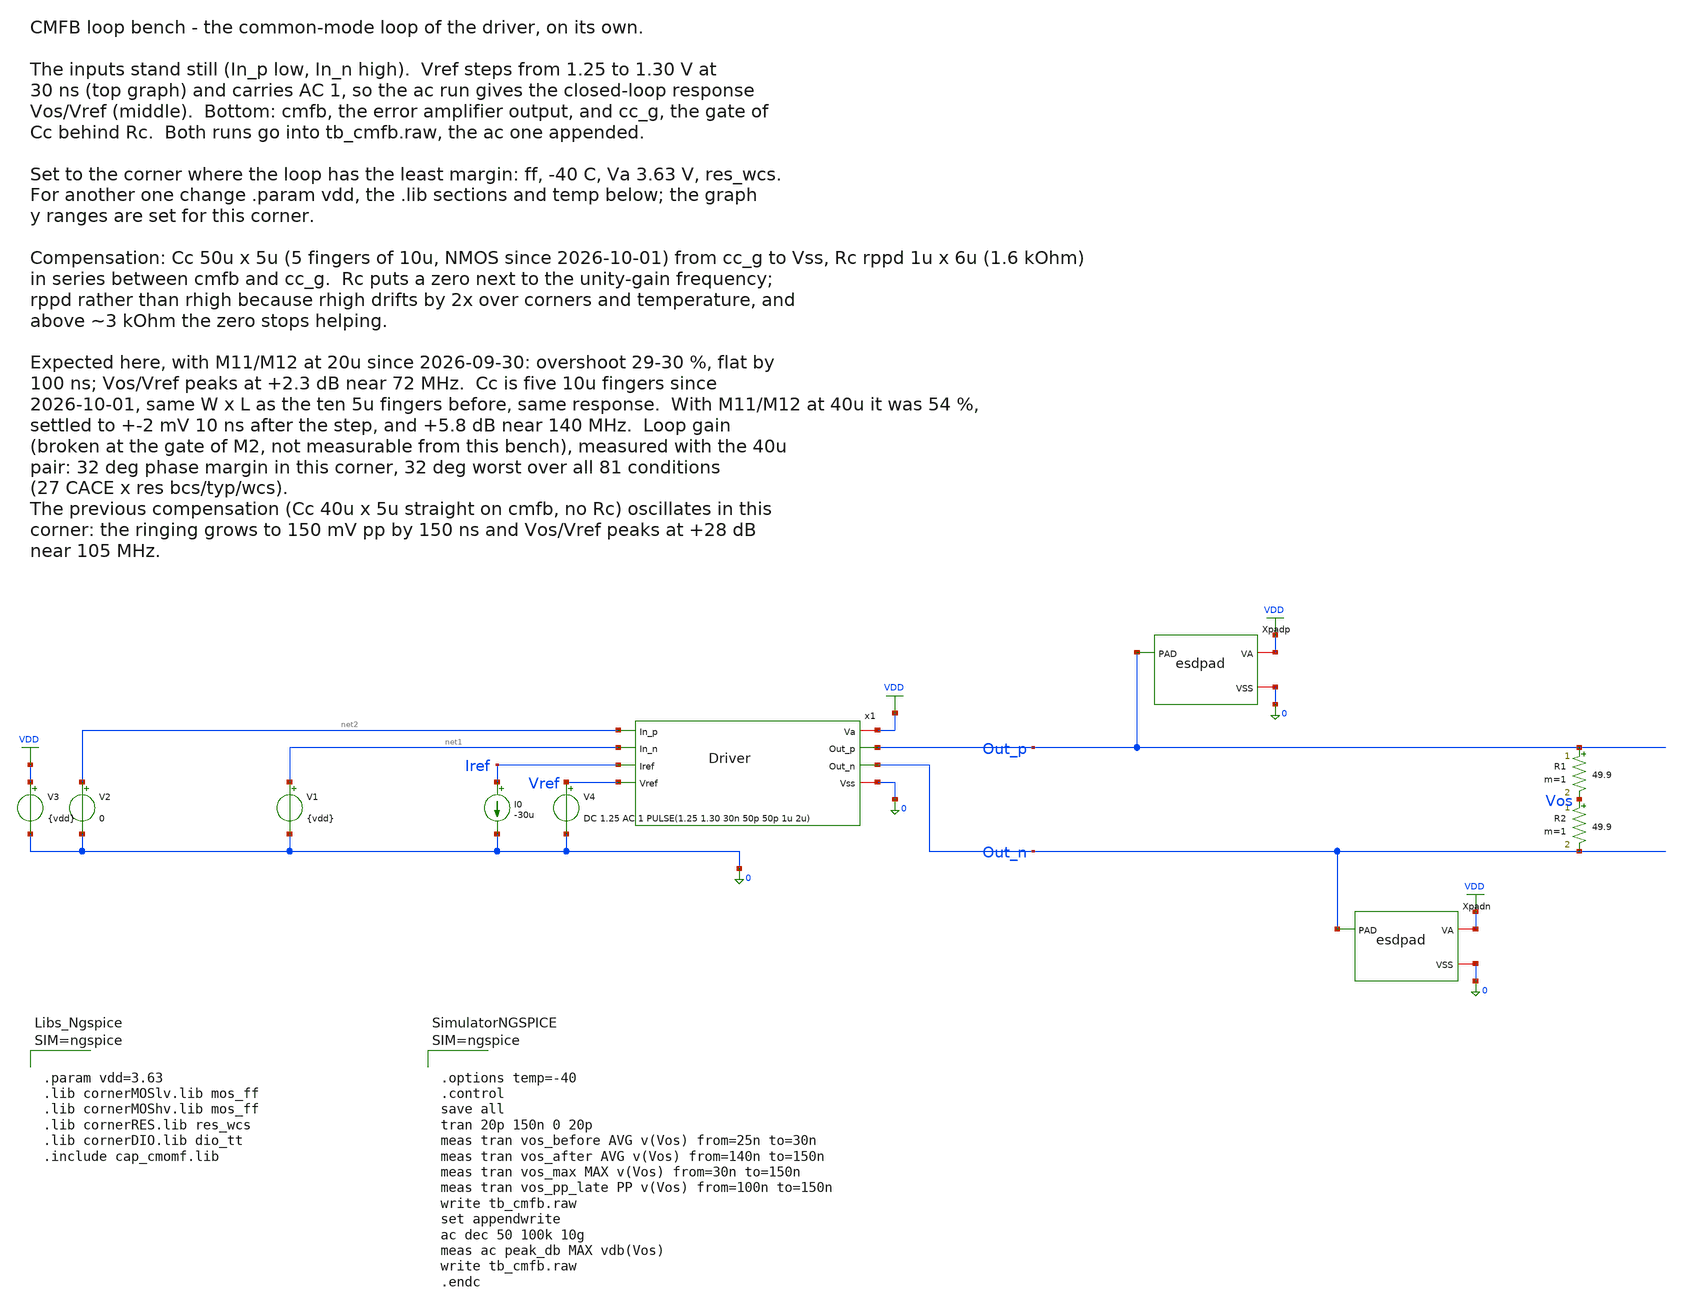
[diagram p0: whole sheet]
** sch_path: macros/lvds_tx/testbenches/xschem/tb_cmfb.sch
**.subckt tb_cmfb
x1 VDD Out_p net2 net1 Iref Vref Out_n 0 Driver
Xpadp Out_p VDD 0 esdpad
Xpadn Out_n VDD 0 esdpad
R1 Out_p Vos 49.9 m=1
R2 Vos Out_n 49.9 m=1
I0 Iref 0 -30u
V1 net1 0 {vdd}
V2 net2 0 0
V3 VDD 0 {vdd}
V4 Vref 0 DC 1.25 AC 1 PULSE(1.25 1.30 30n 50p 50p 1u 2u)
**** begin user architecture code



.param vdd=3.63
.lib cornerMOSlv.lib mos_ff
.lib cornerMOShv.lib mos_ff
.lib cornerRES.lib res_wcs
.lib cornerDIO.lib dio_tt
.include cap_cmomf.lib






.options temp=-40
.control
save all
tran 20p 150n 0 20p
meas tran vos_before AVG v(Vos) from=25n to=30n
meas tran vos_after AVG v(Vos) from=140n to=150n
meas tran vos_max MAX v(Vos) from=30n to=150n
meas tran vos_pp_late PP v(Vos) from=100n to=150n
write tb_cmfb.raw
set appendwrite
ac dec 50 100k 10g
meas ac peak_db MAX vdb(Vos)
write tb_cmfb.raw
.endc



**** end user architecture code
**.ends

* expanding   symbol:  Driver.sym # of pins=8
** sym_path: macros/lvds_tx/schematic/xschem/Driver.sym
** sch_path: macros/lvds_tx/schematic/xschem/Driver.sch
.subckt Driver Va Out_p In_p In_n Iref Vref Out_n Vss
*.iopin Va
*.opin Out_p
*.opin Out_n
*.ipin Vref
*.ipin In_p
*.ipin In_n
*.iopin Vss
*.ipin Iref
XM9 Iref Iref Vss Vss sg13_hv_nmos w=0.8u l=0.5u ng=1 m=1 mm_ok=1
XCop Vss Out_p Vss Vss sg13_hv_nmos w=20u l=5u ng=2 m=1 mm_ok=1
XCon Vss Out_n Vss Vss sg13_hv_nmos w=20u l=5u ng=2 m=1 mm_ok=1
x_cmfb cm Vref Iref cmfb Va Vss cmfb_amp
x_hbridge In_p In_n Iref cmfb Out_p Out_n cm Va Vss hbridge
.ends


* expanding   symbol:  esdpad.sym # of pins=3
** sym_path: macros/lvds_tx/schematic/xschem/esdpad.sym
** sch_path: macros/lvds_tx/schematic/xschem/esdpad.sch
.subckt esdpad PAD VA VSS
*.iopin PAD
*.iopin VA
*.iopin VSS
XDdvdd VA PAD VSS diodevdd_4kv m=1
XDdvss VA PAD VSS diodevss_4kv m=1
Cpad PAD VSS 90f m=1
.ends


* expanding   symbol:  cmfb_amp.sym # of pins=6
** sym_path: macros/lvds_tx/schematic/xschem/cmfb_amp.sym
** sch_path: macros/lvds_tx/schematic/xschem/cmfb_amp.sch
.subckt cmfb_amp cm Vref Iref cmfb Va Vss
*.iopin Va
*.iopin Vss
*.ipin cm
*.ipin Iref
*.ipin Vref
*.opin cmfb
XM13 pd pd Va Va sg13_hv_pmos w=5u l=1u ng=1 m=1 mm_ok=1
XM14 cmfb pd Va Va sg13_hv_pmos w=5u l=1u ng=1 m=1 mm_ok=1
XM11 pd cm otail Vss sg13_hv_nmos w=20u l=1u ng=4 m=1 mm_ok=1
XM12 cmfb Vref otail Vss sg13_hv_nmos w=20u l=1u ng=4 m=1 mm_ok=1
XM10 otail Iref Vss Vss sg13_hv_nmos w=0.8u l=0.5u ng=1 m=1 mm_ok=1
XCc Vss cc_g Vss Vss sg13_hv_nmos w=50u l=5u ng=5 m=1 mm_ok=1
XRc cmfb cc_g Vss rppd w=1u l=6u m=1 b=0 mm_ok=1
.ends


* expanding   symbol:  hbridge.sym # of pins=9
** sym_path: macros/lvds_tx/schematic/xschem/hbridge.sym
** sch_path: macros/lvds_tx/schematic/xschem/hbridge.sch
.subckt hbridge In_p In_n Iref cmfb Out_p Out_n cm Va Vss
*.iopin Va
*.iopin Vss
*.ipin In_p
*.ipin In_n
*.ipin Iref
*.ipin cmfb
*.opin Out_p
*.opin Out_n
*.opin cm
XCtn Vss tail_n Vss Vss sg13_hv_nmos w=30u l=5u ng=3 m=1 mm_ok=1
XM2 tail_p cmfb Va Va sg13_hv_pmos w=97.2u l=0.5u ng=20 m=1 mm_ok=1
XM5 Out_p In_p tail_p Va sg13_hv_pmos w=80u l=0.4u ng=16 m=1 mm_ok=1
XM4 Out_n In_n tail_p Va sg13_hv_pmos w=80u l=0.4u ng=16 m=1 mm_ok=1
XM1 Out_p In_p tail_n Vss sg13_hv_nmos w=30u l=0.45u ng=15 m=1 mm_ok=1
XM3 Out_n In_n tail_n Vss sg13_hv_nmos w=30u l=0.45u ng=15 m=1 mm_ok=1
XM6 tail_n Iref Vss Vss sg13_hv_nmos w=99.2u l=0.5u ng=31 m=1 mm_ok=1
XRp Out_p cm Vss rhigh w=1u l=7.35u m=1 b=0 mm_ok=1
XRn Out_n cm Vss rhigh w=1u l=7.35u m=1 b=0 mm_ok=1
.ends

.GLOBAL VDD
.end
